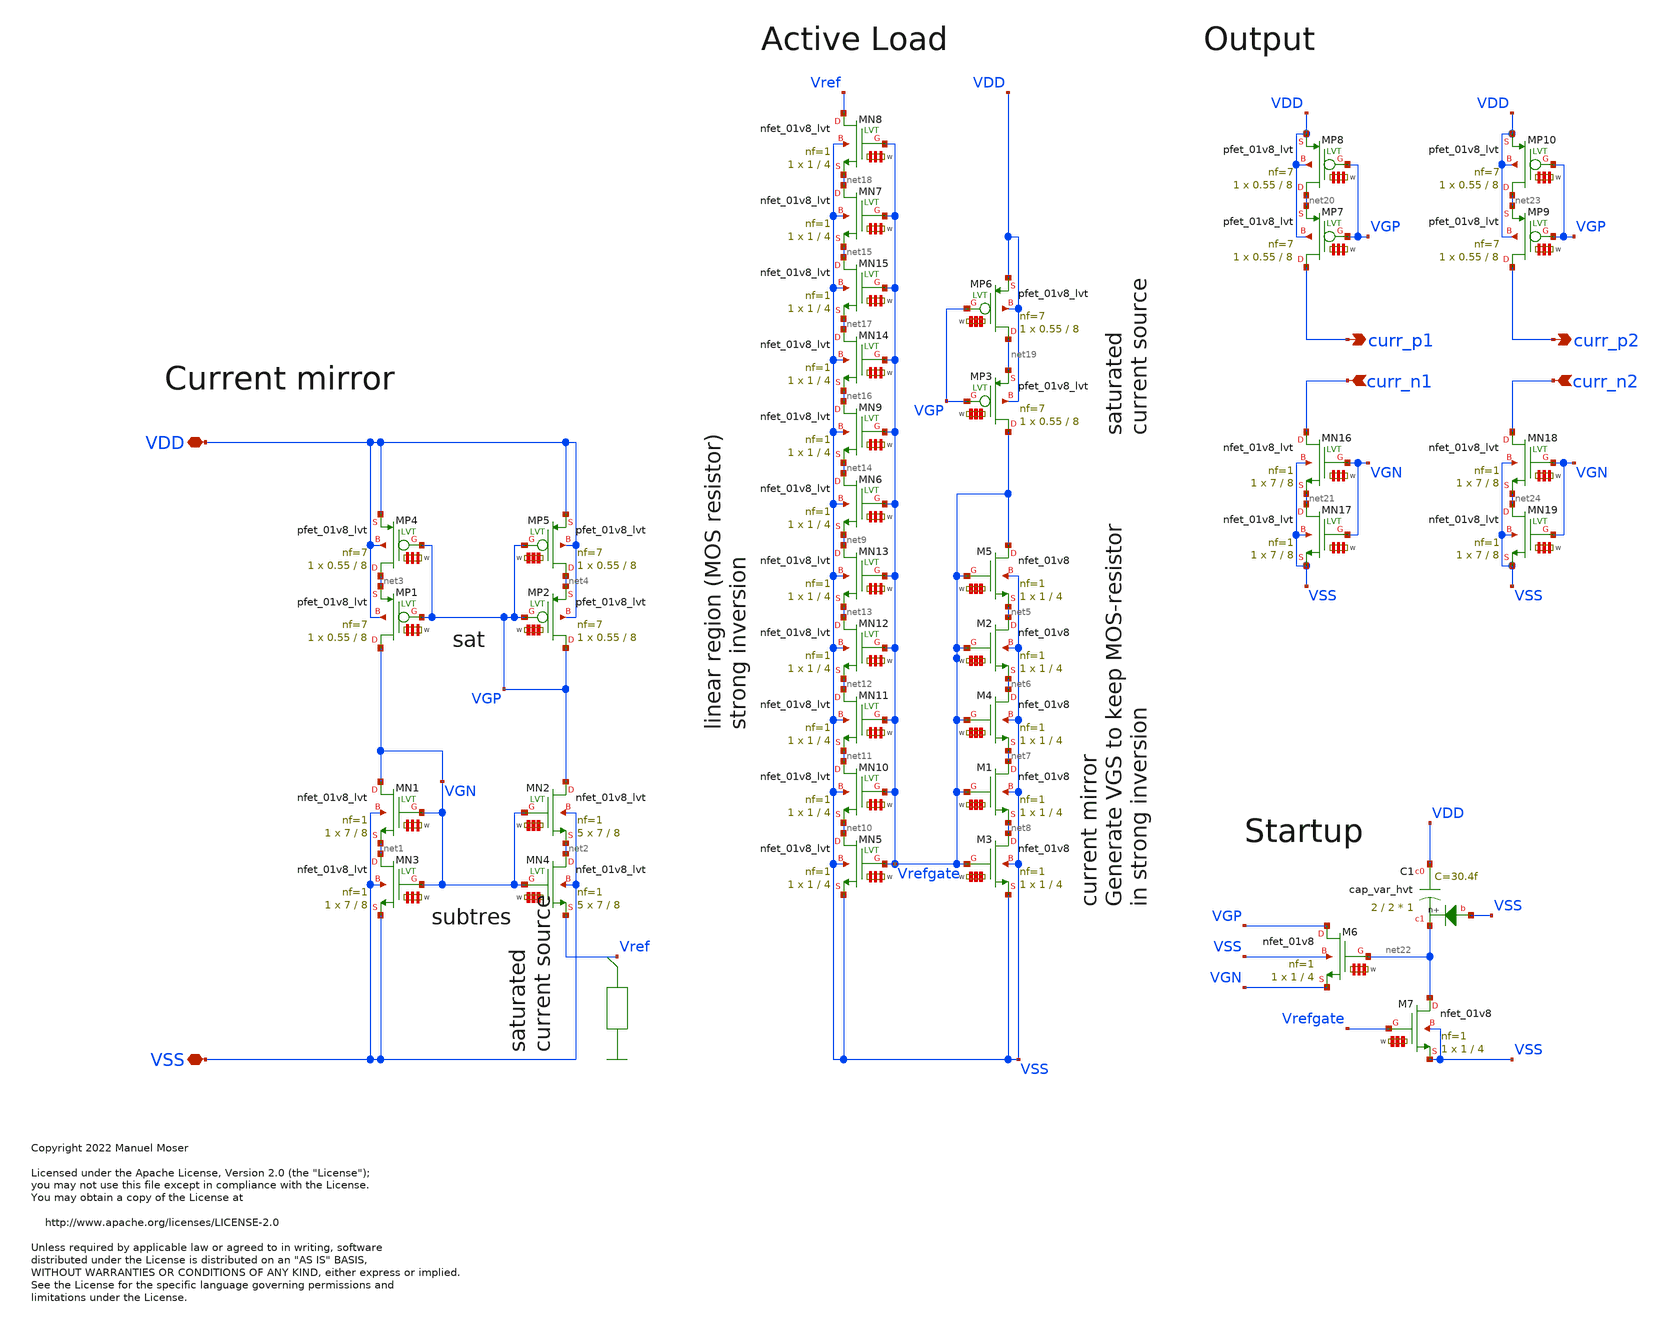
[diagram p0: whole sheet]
** sch_path: xschem/ldo_isource.sch
* Copyright 2022 Manuel Moser
* Licensed under the Apache License, Version 2.0 (the "License");
**.subckt ldo_isource VDD VSS curr_n1 curr_p1 curr_n2 curr_p2
*.iopin VDD
*.iopin VSS
*.ipin curr_n1
*.opin curr_p1
*.ipin curr_n2
*.opin curr_p2
XMP2 VGP VGP net4 VDD sky130_fd_pr__pfet_01v8_lvt L=8 W='0.55 * 7 ' nf=7 ad='int((nf+1)/2) * W / nf * 0.29'
+ as='int((nf+2)/2) * W / nf * 0.29' pd='2*int((nf+1)/2) * (W / nf + 0.29)' ps='2*int((nf+2)/2) * (W / nf + 0.29)'
+ nrd='0.29 / W ' nrs='0.29 / W ' sa=0 sb=0 sd=0 mult=1 m=1
XMP1 VGN VGP net3 VDD sky130_fd_pr__pfet_01v8_lvt L=8 W='0.55 * 7 ' nf=7 ad='int((nf+1)/2) * W / nf * 0.29'
+ as='int((nf+2)/2) * W / nf * 0.29' pd='2*int((nf+1)/2) * (W / nf + 0.29)' ps='2*int((nf+2)/2) * (W / nf + 0.29)'
+ nrd='0.29 / W ' nrs='0.29 / W ' sa=0 sb=0 sd=0 mult=1 m=1
XMN1 VGN VGN net1 VSS sky130_fd_pr__nfet_01v8_lvt L=8 W='7 * 1 ' nf=1 ad='int((nf+1)/2) * W / nf * 0.29'
+ as='int((nf+2)/2) * W / nf * 0.29' pd='2*int((nf+1)/2) * (W / nf + 0.29)' ps='2*int((nf+2)/2) * (W / nf + 0.29)'
+ nrd='0.29 / W ' nrs='0.29 / W ' sa=0 sb=0 sd=0 mult=1 m=1
XMN2 VGP VGN net2 VSS sky130_fd_pr__nfet_01v8_lvt L=8 W='7 * 1 ' nf=1 ad='int((nf+1)/2) * W / nf * 0.29'
+ as='int((nf+2)/2) * W / nf * 0.29' pd='2*int((nf+1)/2) * (W / nf + 0.29)' ps='2*int((nf+2)/2) * (W / nf + 0.29)'
+ nrd='0.29 / W ' nrs='0.29 / W ' sa=0 sb=0 sd=0 mult=5 m=5
XMN3 net1 VGN VSS VSS sky130_fd_pr__nfet_01v8_lvt L=8 W='7 * 1 ' nf=1 ad='int((nf+1)/2) * W / nf * 0.29'
+ as='int((nf+2)/2) * W / nf * 0.29' pd='2*int((nf+1)/2) * (W / nf + 0.29)' ps='2*int((nf+2)/2) * (W / nf + 0.29)'
+ nrd='0.29 / W ' nrs='0.29 / W ' sa=0 sb=0 sd=0 mult=1 m=1
XMN4 net2 VGN Vref VSS sky130_fd_pr__nfet_01v8_lvt L=8 W='7 * 1 ' nf=1 ad='int((nf+1)/2) * W / nf * 0.29'
+ as='int((nf+2)/2) * W / nf * 0.29' pd='2*int((nf+1)/2) * (W / nf + 0.29)' ps='2*int((nf+2)/2) * (W / nf + 0.29)'
+ nrd='0.29 / W ' nrs='0.29 / W ' sa=0 sb=0 sd=0 mult=5 m=5
XMP4 net3 VGP VDD VDD sky130_fd_pr__pfet_01v8_lvt L=8 W='0.55 * 7 ' nf=7 ad='int((nf+1)/2) * W / nf * 0.29'
+ as='int((nf+2)/2) * W / nf * 0.29' pd='2*int((nf+1)/2) * (W / nf + 0.29)' ps='2*int((nf+2)/2) * (W / nf + 0.29)'
+ nrd='0.29 / W ' nrs='0.29 / W ' sa=0 sb=0 sd=0 mult=1 m=1
XMP5 net4 VGP VDD VDD sky130_fd_pr__pfet_01v8_lvt L=8 W='0.55 * 7 ' nf=7 ad='int((nf+1)/2) * W / nf * 0.29'
+ as='int((nf+2)/2) * W / nf * 0.29' pd='2*int((nf+1)/2) * (W / nf + 0.29)' ps='2*int((nf+2)/2) * (W / nf + 0.29)'
+ nrd='0.29 / W ' nrs='0.29 / W ' sa=0 sb=0 sd=0 mult=1 m=1
XMP3 Vrefgate VGP net19 VDD sky130_fd_pr__pfet_01v8_lvt L=8 W='0.55 * 7 ' nf=7 ad='int((nf+1)/2) * W / nf * 0.29'
+ as='int((nf+2)/2) * W / nf * 0.29' pd='2*int((nf+1)/2) * (W / nf + 0.29)' ps='2*int((nf+2)/2) * (W / nf + 0.29)'
+ nrd='0.29 / W ' nrs='0.29 / W ' sa=0 sb=0 sd=0 mult=1 m=1
XM2 net5 Vrefgate net6 VSS sky130_fd_pr__nfet_01v8 L=4 W='1 * 1 ' nf=1 ad='int((nf+1)/2) * W / nf * 0.29'
+ as='int((nf+2)/2) * W / nf * 0.29' pd='2*int((nf+1)/2) * (W / nf + 0.29)' ps='2*int((nf+2)/2) * (W / nf + 0.29)'
+ nrd='0.29 / W ' nrs='0.29 / W ' sa=0 sb=0 sd=0 mult=1 m=1
XM3 net8 Vrefgate VSS VSS sky130_fd_pr__nfet_01v8 L=4 W='1 * 1 ' nf=1 ad='int((nf+1)/2) * W / nf * 0.29'
+ as='int((nf+2)/2) * W / nf * 0.29' pd='2*int((nf+1)/2) * (W / nf + 0.29)' ps='2*int((nf+2)/2) * (W / nf + 0.29)'
+ nrd='0.29 / W ' nrs='0.29 / W ' sa=0 sb=0 sd=0 mult=1 m=1
XM1 net7 Vrefgate net8 VSS sky130_fd_pr__nfet_01v8 L=4 W='1 * 1 ' nf=1 ad='int((nf+1)/2) * W / nf * 0.29'
+ as='int((nf+2)/2) * W / nf * 0.29' pd='2*int((nf+1)/2) * (W / nf + 0.29)' ps='2*int((nf+2)/2) * (W / nf + 0.29)'
+ nrd='0.29 / W ' nrs='0.29 / W ' sa=0 sb=0 sd=0 mult=1 m=1
XM4 net6 Vrefgate net7 VSS sky130_fd_pr__nfet_01v8 L=4 W='1 * 1 ' nf=1 ad='int((nf+1)/2) * W / nf * 0.29'
+ as='int((nf+2)/2) * W / nf * 0.29' pd='2*int((nf+1)/2) * (W / nf + 0.29)' ps='2*int((nf+2)/2) * (W / nf + 0.29)'
+ nrd='0.29 / W ' nrs='0.29 / W ' sa=0 sb=0 sd=0 mult=1 m=1
XMN5 net10 Vrefgate VSS VSS sky130_fd_pr__nfet_01v8_lvt L=4 W='1 * 1 ' nf=1 ad='int((nf+1)/2) * W / nf * 0.29'
+ as='int((nf+2)/2) * W / nf * 0.29' pd='2*int((nf+1)/2) * (W / nf + 0.29)' ps='2*int((nf+2)/2) * (W / nf + 0.29)'
+ nrd='0.29 / W ' nrs='0.29 / W ' sa=0 sb=0 sd=0 mult=1 m=1
XMN6 net14 Vrefgate net9 VSS sky130_fd_pr__nfet_01v8_lvt L=4 W='1 * 1 ' nf=1 ad='int((nf+1)/2) * W / nf * 0.29'
+ as='int((nf+2)/2) * W / nf * 0.29' pd='2*int((nf+1)/2) * (W / nf + 0.29)' ps='2*int((nf+2)/2) * (W / nf + 0.29)'
+ nrd='0.29 / W ' nrs='0.29 / W ' sa=0 sb=0 sd=0 mult=1 m=1
XMN9 net16 Vrefgate net14 VSS sky130_fd_pr__nfet_01v8_lvt L=4 W='1 * 1 ' nf=1 ad='int((nf+1)/2) * W / nf * 0.29'
+ as='int((nf+2)/2) * W / nf * 0.29' pd='2*int((nf+1)/2) * (W / nf + 0.29)' ps='2*int((nf+2)/2) * (W / nf + 0.29)'
+ nrd='0.29 / W ' nrs='0.29 / W ' sa=0 sb=0 sd=0 mult=1 m=1
XM5 Vrefgate Vrefgate net5 VSS sky130_fd_pr__nfet_01v8 L=4 W='1 * 1 ' nf=1 ad='int((nf+1)/2) * W / nf * 0.29'
+ as='int((nf+2)/2) * W / nf * 0.29' pd='2*int((nf+1)/2) * (W / nf + 0.29)' ps='2*int((nf+2)/2) * (W / nf + 0.29)'
+ nrd='0.29 / W ' nrs='0.29 / W ' sa=0 sb=0 sd=0 mult=1 m=1
XMN10 net11 Vrefgate net10 VSS sky130_fd_pr__nfet_01v8_lvt L=4 W='1 * 1 ' nf=1 ad='int((nf+1)/2) * W / nf * 0.29'
+ as='int((nf+2)/2) * W / nf * 0.29' pd='2*int((nf+1)/2) * (W / nf + 0.29)' ps='2*int((nf+2)/2) * (W / nf + 0.29)'
+ nrd='0.29 / W ' nrs='0.29 / W ' sa=0 sb=0 sd=0 mult=1 m=1
XMN11 net12 Vrefgate net11 VSS sky130_fd_pr__nfet_01v8_lvt L=4 W='1 * 1 ' nf=1 ad='int((nf+1)/2) * W / nf * 0.29'
+ as='int((nf+2)/2) * W / nf * 0.29' pd='2*int((nf+1)/2) * (W / nf + 0.29)' ps='2*int((nf+2)/2) * (W / nf + 0.29)'
+ nrd='0.29 / W ' nrs='0.29 / W ' sa=0 sb=0 sd=0 mult=1 m=1
XMN12 net13 Vrefgate net12 VSS sky130_fd_pr__nfet_01v8_lvt L=4 W='1 * 1 ' nf=1 ad='int((nf+1)/2) * W / nf * 0.29'
+ as='int((nf+2)/2) * W / nf * 0.29' pd='2*int((nf+1)/2) * (W / nf + 0.29)' ps='2*int((nf+2)/2) * (W / nf + 0.29)'
+ nrd='0.29 / W ' nrs='0.29 / W ' sa=0 sb=0 sd=0 mult=1 m=1
XMN13 net9 Vrefgate net13 VSS sky130_fd_pr__nfet_01v8_lvt L=4 W='1 * 1 ' nf=1 ad='int((nf+1)/2) * W / nf * 0.29'
+ as='int((nf+2)/2) * W / nf * 0.29' pd='2*int((nf+1)/2) * (W / nf + 0.29)' ps='2*int((nf+2)/2) * (W / nf + 0.29)'
+ nrd='0.29 / W ' nrs='0.29 / W ' sa=0 sb=0 sd=0 mult=1 m=1
XMN7 net18 Vrefgate net15 VSS sky130_fd_pr__nfet_01v8_lvt L=4 W='1 * 1 ' nf=1 ad='int((nf+1)/2) * W / nf * 0.29'
+ as='int((nf+2)/2) * W / nf * 0.29' pd='2*int((nf+1)/2) * (W / nf + 0.29)' ps='2*int((nf+2)/2) * (W / nf + 0.29)'
+ nrd='0.29 / W ' nrs='0.29 / W ' sa=0 sb=0 sd=0 mult=1 m=1
XMN8 Vref Vrefgate net18 VSS sky130_fd_pr__nfet_01v8_lvt L=4 W='1 * 1 ' nf=1 ad='int((nf+1)/2) * W / nf * 0.29'
+ as='int((nf+2)/2) * W / nf * 0.29' pd='2*int((nf+1)/2) * (W / nf + 0.29)' ps='2*int((nf+2)/2) * (W / nf + 0.29)'
+ nrd='0.29 / W ' nrs='0.29 / W ' sa=0 sb=0 sd=0 mult=1 m=1
XMN14 net17 Vrefgate net16 VSS sky130_fd_pr__nfet_01v8_lvt L=4 W='1 * 1 ' nf=1 ad='int((nf+1)/2) * W / nf * 0.29'
+ as='int((nf+2)/2) * W / nf * 0.29' pd='2*int((nf+1)/2) * (W / nf + 0.29)' ps='2*int((nf+2)/2) * (W / nf + 0.29)'
+ nrd='0.29 / W ' nrs='0.29 / W ' sa=0 sb=0 sd=0 mult=1 m=1
XMN15 net15 Vrefgate net17 VSS sky130_fd_pr__nfet_01v8_lvt L=4 W='1 * 1 ' nf=1 ad='int((nf+1)/2) * W / nf * 0.29'
+ as='int((nf+2)/2) * W / nf * 0.29' pd='2*int((nf+1)/2) * (W / nf + 0.29)' ps='2*int((nf+2)/2) * (W / nf + 0.29)'
+ nrd='0.29 / W ' nrs='0.29 / W ' sa=0 sb=0 sd=0 mult=1 m=1
XMP6 net19 VGP VDD VDD sky130_fd_pr__pfet_01v8_lvt L=8 W='0.55 * 7 ' nf=7 ad='int((nf+1)/2) * W / nf * 0.29'
+ as='int((nf+2)/2) * W / nf * 0.29' pd='2*int((nf+1)/2) * (W / nf + 0.29)' ps='2*int((nf+2)/2) * (W / nf + 0.29)'
+ nrd='0.29 / W ' nrs='0.29 / W ' sa=0 sb=0 sd=0 mult=1 m=1
XMP7 curr_p1 VGP net20 VDD sky130_fd_pr__pfet_01v8_lvt L=8 W='0.55 * 7 ' nf=7 ad='int((nf+1)/2) * W / nf * 0.29'
+ as='int((nf+2)/2) * W / nf * 0.29' pd='2*int((nf+1)/2) * (W / nf + 0.29)' ps='2*int((nf+2)/2) * (W / nf + 0.29)'
+ nrd='0.29 / W ' nrs='0.29 / W ' sa=0 sb=0 sd=0 mult=1 m=1
XMP8 net20 VGP VDD VDD sky130_fd_pr__pfet_01v8_lvt L=8 W='0.55 * 7 ' nf=7 ad='int((nf+1)/2) * W / nf * 0.29'
+ as='int((nf+2)/2) * W / nf * 0.29' pd='2*int((nf+1)/2) * (W / nf + 0.29)' ps='2*int((nf+2)/2) * (W / nf + 0.29)'
+ nrd='0.29 / W ' nrs='0.29 / W ' sa=0 sb=0 sd=0 mult=1 m=1
XMN16 curr_n1 VGN net21 VSS sky130_fd_pr__nfet_01v8_lvt L=8 W='7 * 1 ' nf=1 ad='int((nf+1)/2) * W / nf * 0.29'
+ as='int((nf+2)/2) * W / nf * 0.29' pd='2*int((nf+1)/2) * (W / nf + 0.29)' ps='2*int((nf+2)/2) * (W / nf + 0.29)'
+ nrd='0.29 / W ' nrs='0.29 / W ' sa=0 sb=0 sd=0 mult=1 m=1
XMN17 net21 VGN VSS VSS sky130_fd_pr__nfet_01v8_lvt L=8 W='7 * 1 ' nf=1 ad='int((nf+1)/2) * W / nf * 0.29'
+ as='int((nf+2)/2) * W / nf * 0.29' pd='2*int((nf+1)/2) * (W / nf + 0.29)' ps='2*int((nf+2)/2) * (W / nf + 0.29)'
+ nrd='0.29 / W ' nrs='0.29 / W ' sa=0 sb=0 sd=0 mult=1 m=1
XM6 VGP net22 VGN VSS sky130_fd_pr__nfet_01v8 L=4 W='1 * 1 ' nf=1 ad='int((nf+1)/2) * W / nf * 0.29'
+ as='int((nf+2)/2) * W / nf * 0.29' pd='2*int((nf+1)/2) * (W / nf + 0.29)' ps='2*int((nf+2)/2) * (W / nf + 0.29)'
+ nrd='0.29 / W ' nrs='0.29 / W ' sa=0 sb=0 sd=0 mult=1 m=1
XM7 net22 Vrefgate VSS VSS sky130_fd_pr__nfet_01v8 L=4 W='1 * 1 ' nf=1 ad='int((nf+1)/2) * W / nf * 0.29'
+ as='int((nf+2)/2) * W / nf * 0.29' pd='2*int((nf+1)/2) * (W / nf + 0.29)' ps='2*int((nf+2)/2) * (W / nf + 0.29)'
+ nrd='0.29 / W ' nrs='0.29 / W ' sa=0 sb=0 sd=0 mult=1 m=1
XC1 VDD net22 VSS sky130_fd_pr__cap_var_hvt W=2 L=2 VM=1 m=1
XMP9 curr_p2 VGP net23 VDD sky130_fd_pr__pfet_01v8_lvt L=8 W='0.55 * 7 ' nf=7 ad='int((nf+1)/2) * W / nf * 0.29'
+ as='int((nf+2)/2) * W / nf * 0.29' pd='2*int((nf+1)/2) * (W / nf + 0.29)' ps='2*int((nf+2)/2) * (W / nf + 0.29)'
+ nrd='0.29 / W ' nrs='0.29 / W ' sa=0 sb=0 sd=0 mult=1 m=1
XMP10 net23 VGP VDD VDD sky130_fd_pr__pfet_01v8_lvt L=8 W='0.55 * 7 ' nf=7 ad='int((nf+1)/2) * W / nf * 0.29'
+ as='int((nf+2)/2) * W / nf * 0.29' pd='2*int((nf+1)/2) * (W / nf + 0.29)' ps='2*int((nf+2)/2) * (W / nf + 0.29)'
+ nrd='0.29 / W ' nrs='0.29 / W ' sa=0 sb=0 sd=0 mult=1 m=1
XMN18 curr_n2 VGN net24 VSS sky130_fd_pr__nfet_01v8_lvt L=8 W='7 * 1 ' nf=1 ad='int((nf+1)/2) * W / nf * 0.29'
+ as='int((nf+2)/2) * W / nf * 0.29' pd='2*int((nf+1)/2) * (W / nf + 0.29)' ps='2*int((nf+2)/2) * (W / nf + 0.29)'
+ nrd='0.29 / W ' nrs='0.29 / W ' sa=0 sb=0 sd=0 mult=1 m=1
XMN19 net24 VGN VSS VSS sky130_fd_pr__nfet_01v8_lvt L=8 W='7 * 1 ' nf=1 ad='int((nf+1)/2) * W / nf * 0.29'
+ as='int((nf+2)/2) * W / nf * 0.29' pd='2*int((nf+1)/2) * (W / nf + 0.29)' ps='2*int((nf+2)/2) * (W / nf + 0.29)'
+ nrd='0.29 / W ' nrs='0.29 / W ' sa=0 sb=0 sd=0 mult=1 m=1
**.ends
.end
